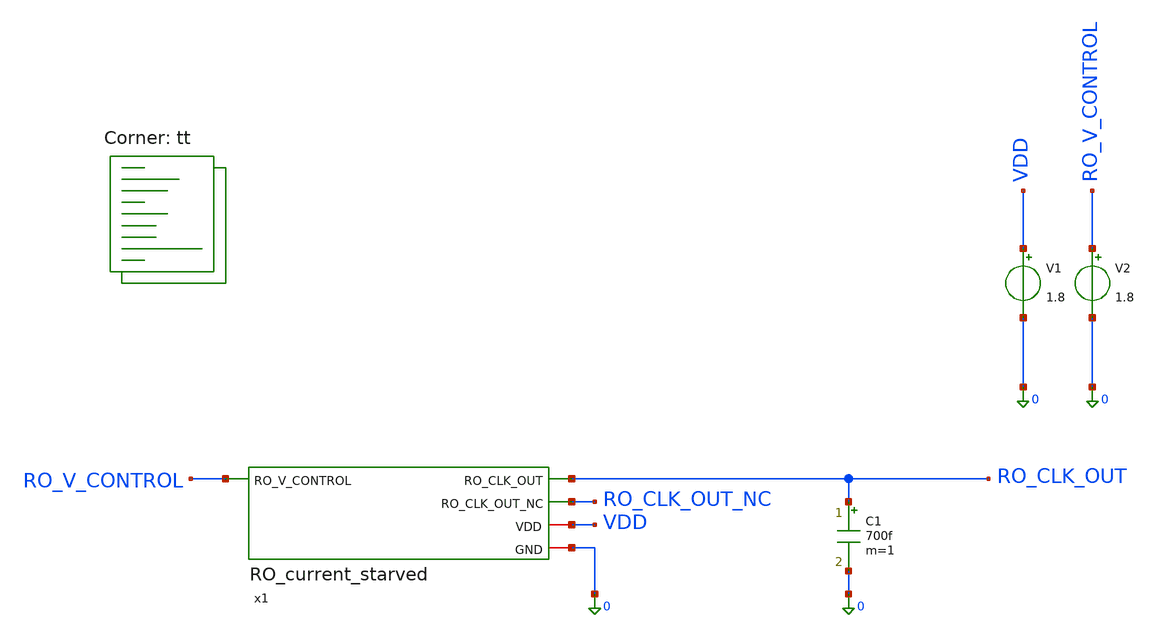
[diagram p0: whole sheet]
** sch_path: src/analog_source_files/RO_current_starved_tb.sch
**.subckt RO_current_starved_tb
x1 RO_CLK_OUT RO_V_CONTROL VDD 0 RO_CLK_OUT_NC RO_current_starved
V1 VDD 0 1.8
V2 RO_V_CONTROL 0 1.8
C1 RO_CLK_OUT 0 700f m=1
**** begin user architecture code
.lib $::SKYWATER_MODELS/sky130.lib.spice tt


.include /foss/pdks/sky130A/libs.ref/sky130_fd_sc_hd/spice/sky130_fd_sc_hd.spice
.ic v(RO_CLK_OUT) = 0V
.control
  setplot new
  set sweep_plot = $curplot
  set curplotname = dcsweep

  let vctrl = unitvec(40)
  let f_osc = unitvec(40)
  let i_vdd = unitvec(40)

  let idx = 0
  let v_curr = 0.4

  while v_curr <= 1.8001
    alter V2 $&v_curr
    tran 0.1n 1000n

    set curr_tran = $curplot
    setplot $sweep_plot

    let v_thresh = v_curr / 2
    set str_v_thresh = $&v_thresh

    if $&idx = 4
      set tran_06 = $curr_tran
    end

    if $&idx = 7
      set tran_07 = $curr_tran
    end

    if $&idx = 10
      set tran_09 = $curr_tran
    end

    setplot $curr_tran
    let t_per = 0

    meas tran t_3per TRIG v(ro_clk_out) VAL=$str_v_thresh RISE=1 TARG v(ro_clk_out)
+ VAL=$str_v_thresh RISE=4 FROM=150n
    meas tran i_avg AVG i(V1) FROM=150n TO=1000n

    if t_3per > 0
      let f_val = 3.0 / t_3per
      set str_f = $&f_val
    else
      set str_f = 0
    end

    let i_val = -i_avg
    set str_i = $&i_val

    setplot $sweep_plot
    let vctrl[$&idx] = $&v_curr
    let f_osc[$&idx] = $str_f
    let i_vdd[$&idx] = $str_i

    let idx = idx + 1
    let v_curr = v_curr + 0.05
  end

  let final_idx = idx - 1
  set str_final_idx = $&final_idx

  let vctrl = vctrl[0, $str_final_idx]
  let f_osc = f_osc[0, $str_final_idx]
  let i_vdd = i_vdd[0, $str_final_idx]

  settype frequency f_osc
  settype current i_vdd
  setscale vctrl
  write RO_current_starved_tb_sweep.raw f_osc i_vdd vctrl

  if $?tran_06
    setplot $tran_06
    write RO_current_starved_tb_tran_06.raw v(ro_clk_out) v(ro_clk_out_nc)
  end

  if $?tran_09
    setplot $tran_09
    write RO_current_starved_tb_tran_09.raw v(ro_clk_out) v(ro_clk_out_nc)
  end
  if $?tran_07
    setplot $tran_07
    write RO_current_starved_tb_tran_07.raw v(ro_clk_out) v(ro_clk_out_nc)
  end
.endc



**** end user architecture code
**.ends
.end
